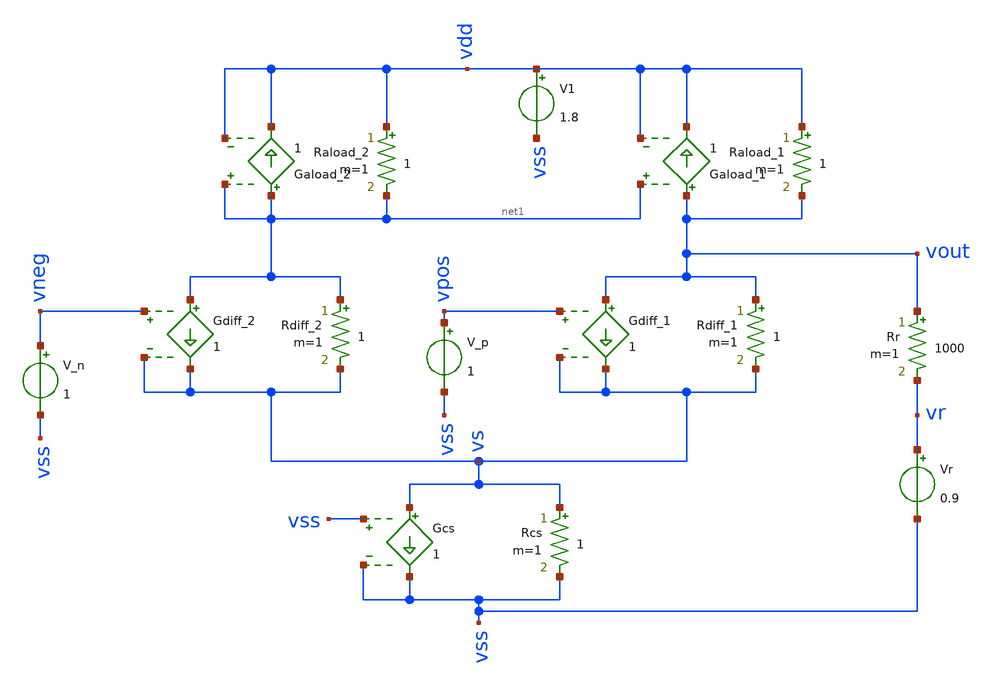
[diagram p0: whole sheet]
** sch_path: test/Tesis_notebooks/xschem/ota_1stage_rout.sch
**.subckt ota_1stage_rout
Rdiff_2 net1 vs 1 m=1
Gdiff_2 net1 vs vneg vs 1
Rdiff_1 vout vs 1 m=1
Gdiff_1 vout vs vpos vs 1
V1 vdd vss 1.8
V_n vneg vss 1
V_p vpos vss 1
Raload_1 vdd vout 1 m=1
Gaload_1 vout vdd net1 vdd 1
Gaload_2 net1 vdd net1 vdd 1
Raload_2 vdd net1 1 m=1
Vr vr vss 0.9
Rr vout vr 1000 m=1
Rcs vs vss 1 m=1
Gcs vs vss vss vss 1
**.ends
.end
